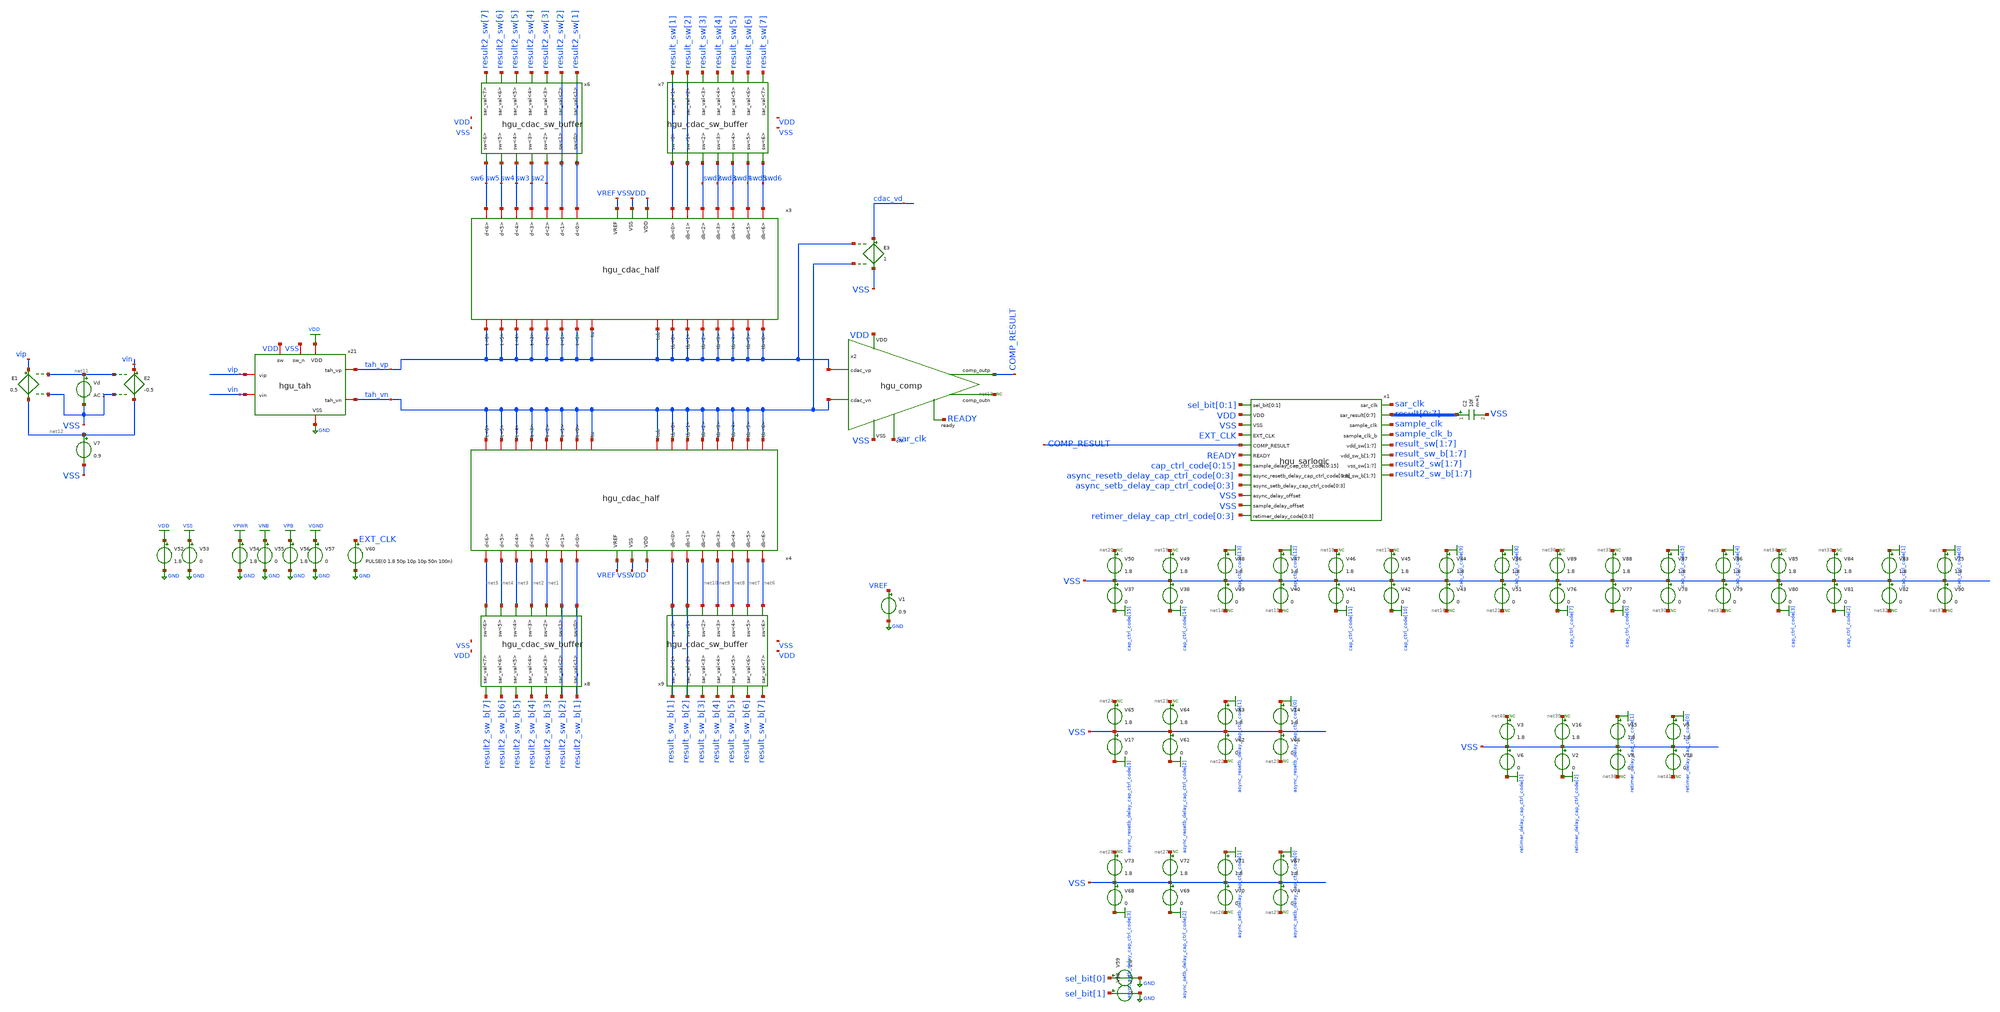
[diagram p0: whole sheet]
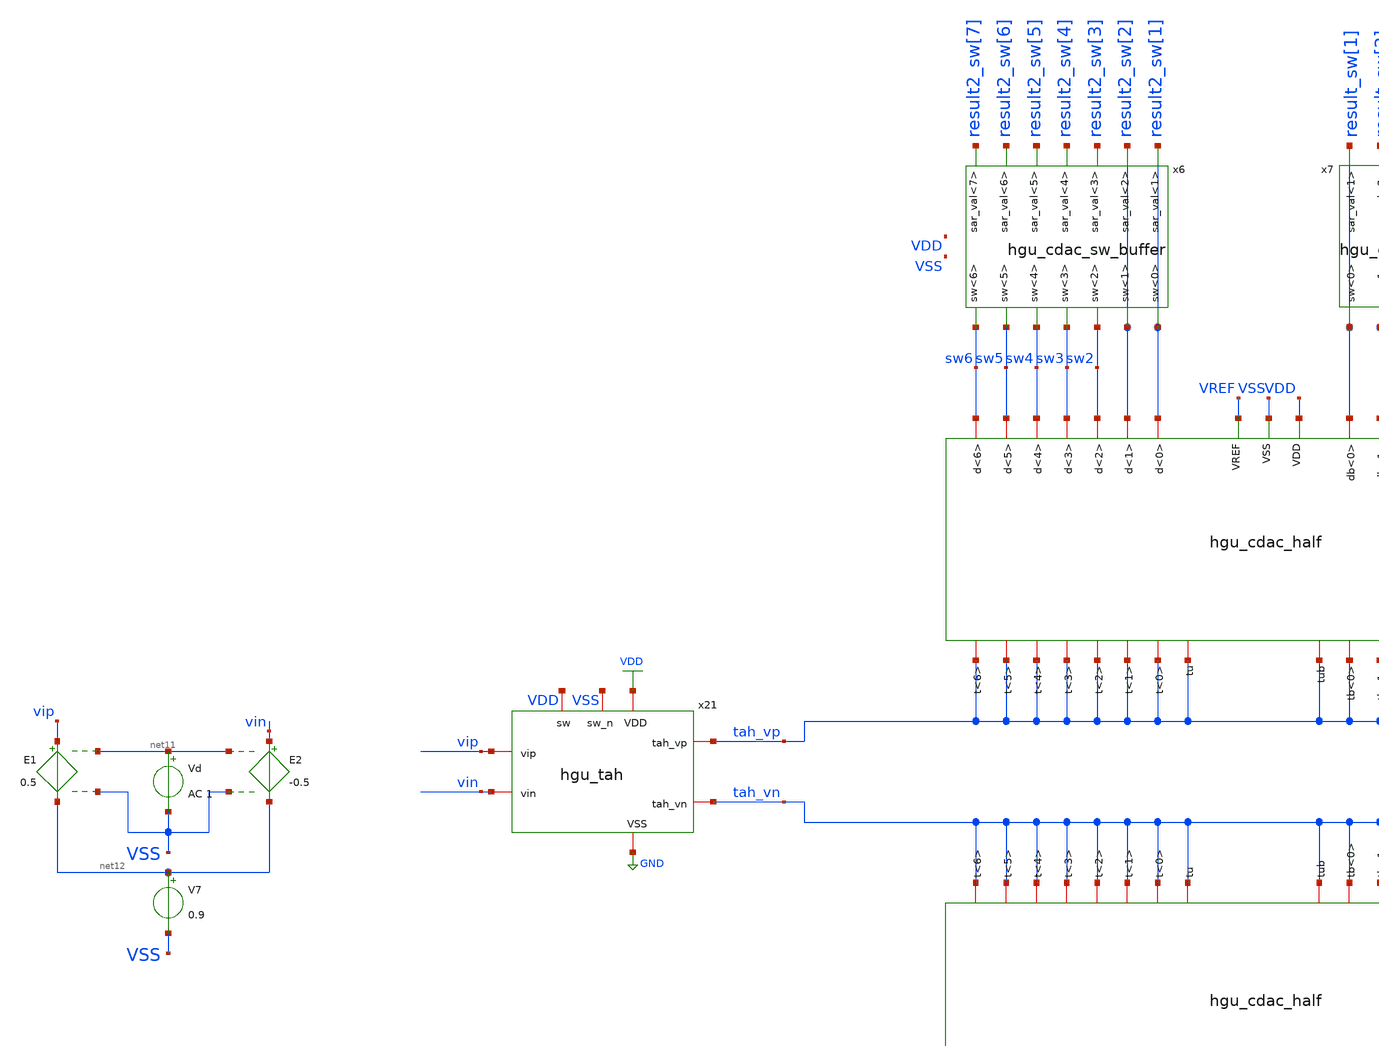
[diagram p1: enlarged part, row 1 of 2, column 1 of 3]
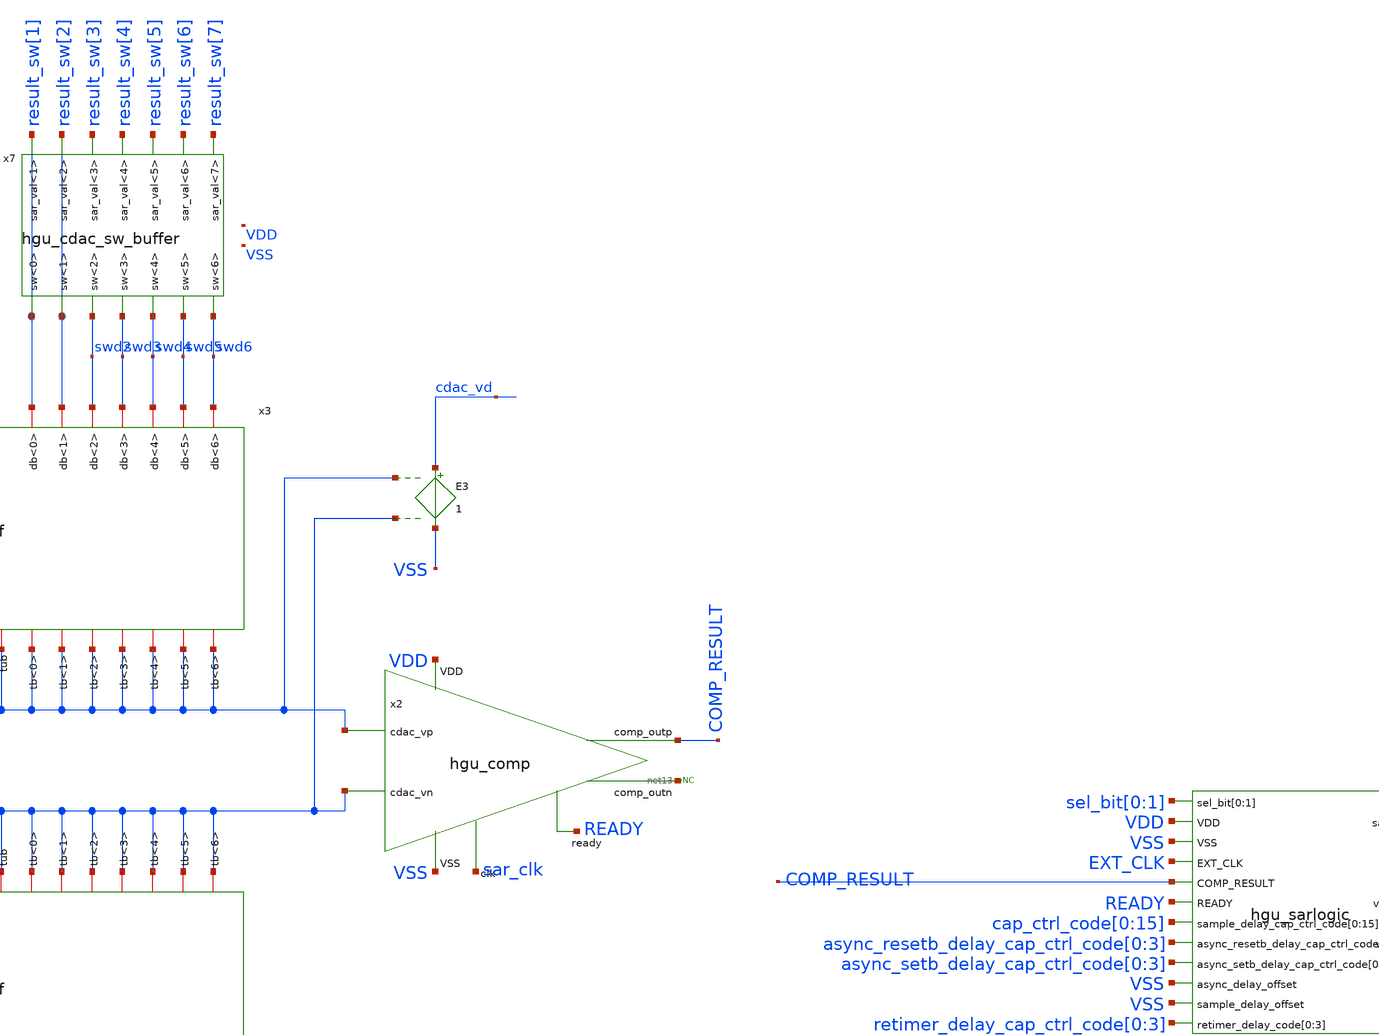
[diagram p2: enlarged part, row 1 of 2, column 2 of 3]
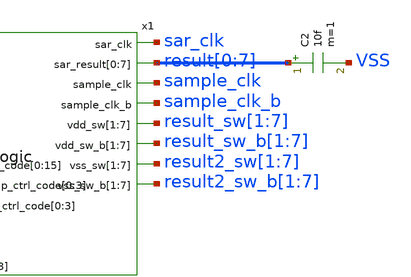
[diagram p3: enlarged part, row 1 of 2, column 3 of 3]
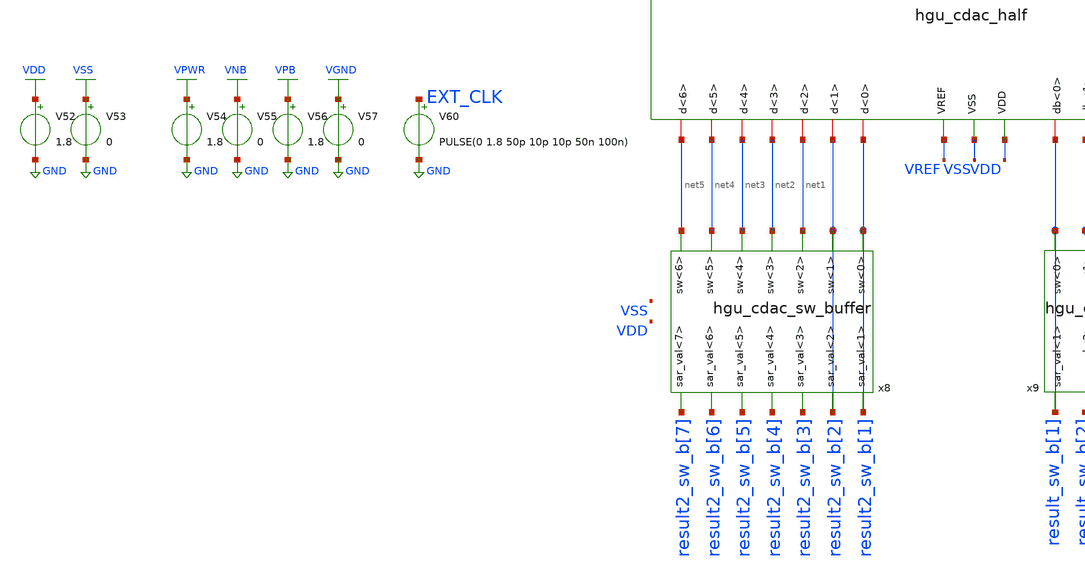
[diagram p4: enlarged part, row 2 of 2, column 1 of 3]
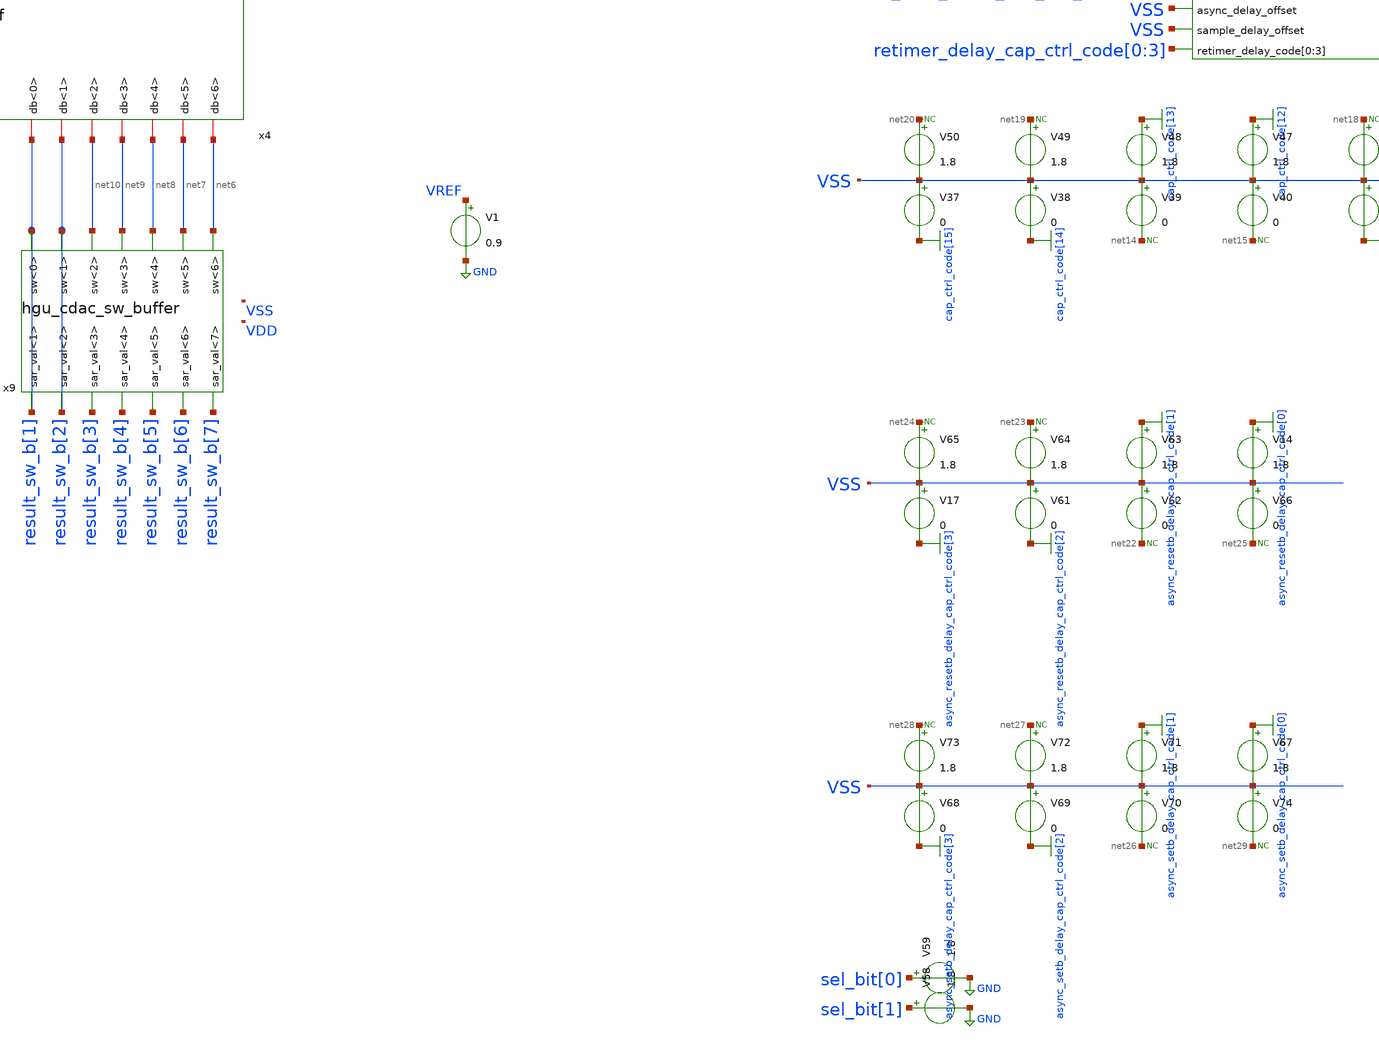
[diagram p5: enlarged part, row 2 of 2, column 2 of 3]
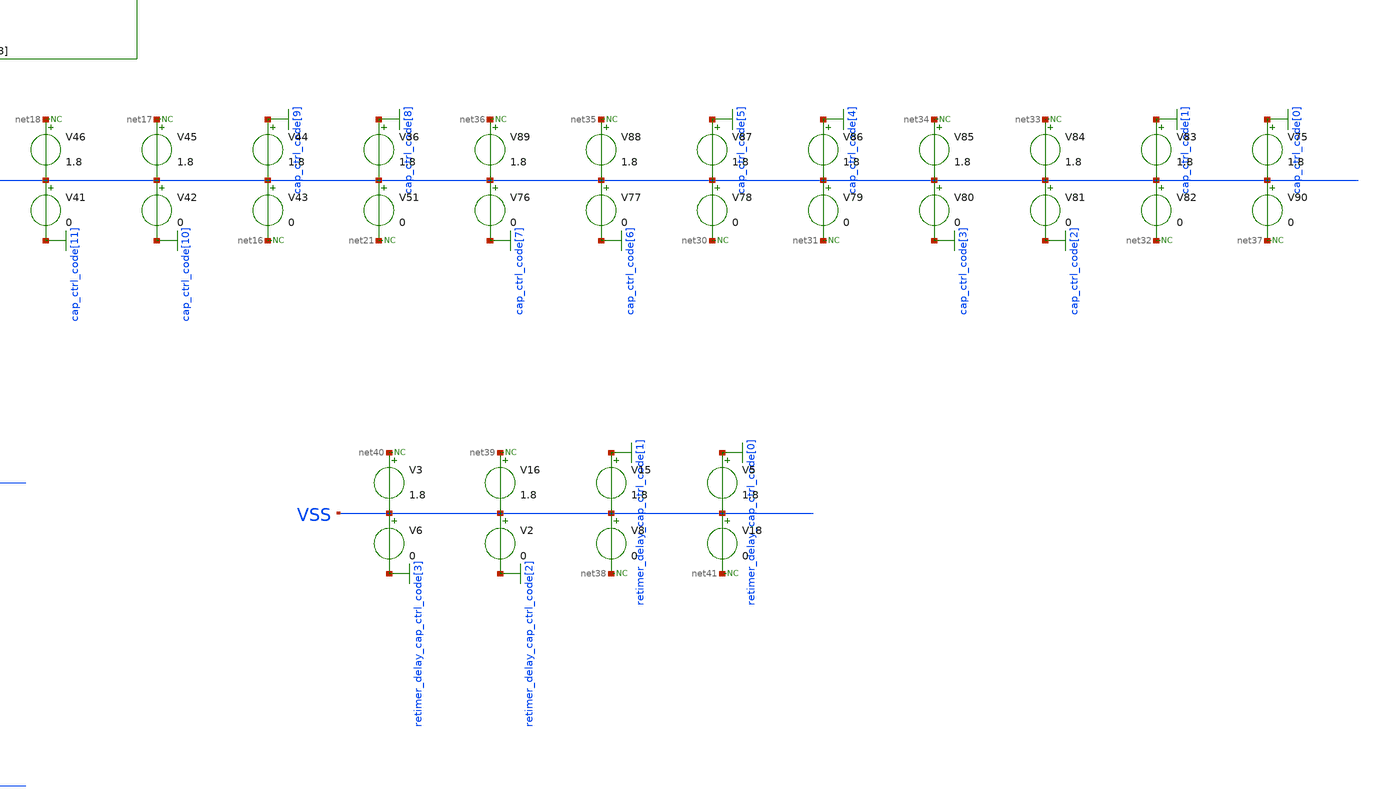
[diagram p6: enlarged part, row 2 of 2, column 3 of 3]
** sch_path: hgu/tb/tb_hgu_AC.sch
**.subckt tb_hgu_AC
x2 READY tah_vn COMP_RESULT net13 tah_vp sar_clk VDD VSS hgu_comp
x3 sw5 swd4 sw3 result_sw[2] swd2 sw2 swd6 swd5 result_sw[1] sw4 sw6 result2_sw[2] result2_sw[1]
+ swd3 VSS VREF tah_vp tah_vp tah_vp tah_vp tah_vp tah_vp tah_vp tah_vp tah_vp tah_vp tah_vp tah_vp tah_vp
+ tah_vp tah_vp tah_vp VDD hgu_cdac_half
x4 net4 net8 net2 result_sw_b[2] net10 net1 net6 net7 result_sw_b[1] net3 net5 result2_sw_b[2]
+ result2_sw_b[1] net9 VSS VREF tah_vn tah_vn tah_vn tah_vn tah_vn tah_vn tah_vn tah_vn tah_vn tah_vn tah_vn tah_vn
+ tah_vn tah_vn tah_vn tah_vn VDD hgu_cdac_half
x21 VDD VDD GND VSS tah_vp vip vin tah_vn hgu_tah
V52 VDD GND 1.8
V53 VSS GND 0
V54 VPWR GND 1.8
V55 VNB GND 0
V56 VPB GND 1.8
V57 VGND GND 0
V60 EXT_CLK GND PULSE(0 1.8 50p 10p 10p 50n 100n)
x6 result2_sw[3] result2_sw[6] result2_sw[1] result2_sw[2] result2_sw[4] result2_sw[5] result2_sw[7]
+ result2_sw[2] sw2 sw5 sw3 result2_sw[1] sw4 sw6 hgu_cdac_sw_buffer
x7 result_sw[3] result_sw[6] result_sw[1] result_sw[2] result_sw[4] result_sw[5] result_sw[7]
+ result_sw[2] swd2 swd5 swd3 result_sw[1] swd4 swd6 hgu_cdac_sw_buffer
x8 result2_sw_b[3] result2_sw_b[6] result2_sw_b[1] result2_sw_b[2] result2_sw_b[4] result2_sw_b[5]
+ result2_sw_b[7] result2_sw_b[2] net1 net4 net2 result2_sw_b[1] net3 net5 hgu_cdac_sw_buffer
x9 result_sw_b[3] result_sw_b[6] result_sw_b[1] result_sw_b[2] result_sw_b[4] result_sw_b[5]
+ result_sw_b[7] result_sw_b[2] net10 net7 net9 result_sw_b[1] net8 net6 hgu_cdac_sw_buffer
V1 VREF GND 0.9
E1 vip net12 net11 VSS 0.5
E2 vin net12 net11 VSS -0.5
Vd net11 VSS AC 1
V7 net12 VSS 0.9
E3 cdac_vd VSS tah_vp tah_vn 1
x1 sar_clk result[0] result[1] result[2] result[3] result[4] result[5] result[6] result[7]
+ sample_clk sel_bit[0] sel_bit[1] sample_clk_b VDD VSS EXT_CLK COMP_RESULT READY result_sw[1] result_sw[2]
+ result_sw[3] result_sw[4] result_sw[5] result_sw[6] result_sw[7] result_sw_b[1] result_sw_b[2] result_sw_b[3]
+ result_sw_b[4] result_sw_b[5] result_sw_b[6] result_sw_b[7] result2_sw[1] result2_sw[2] result2_sw[3]
+ result2_sw[4] result2_sw[5] result2_sw[6] result2_sw[7] result2_sw_b[1] result2_sw_b[2] result2_sw_b[3]
+ result2_sw_b[4] result2_sw_b[5] result2_sw_b[6] result2_sw_b[7] cap_ctrl_code[0] cap_ctrl_code[1] cap_ctrl_code[2]
+ cap_ctrl_code[3] cap_ctrl_code[4] cap_ctrl_code[5] cap_ctrl_code[6] cap_ctrl_code[7] cap_ctrl_code[8]
+ cap_ctrl_code[9] cap_ctrl_code[10] cap_ctrl_code[11] cap_ctrl_code[12] cap_ctrl_code[13] cap_ctrl_code[14]
+ cap_ctrl_code[15] async_resetb_delay_cap_ctrl_code[0] async_resetb_delay_cap_ctrl_code[1]
+ async_resetb_delay_cap_ctrl_code[2] async_resetb_delay_cap_ctrl_code[3] async_setb_delay_cap_ctrl_code[0]
+ async_setb_delay_cap_ctrl_code[1] async_setb_delay_cap_ctrl_code[2] async_setb_delay_cap_ctrl_code[3] VSS VSS
+ retimer_delay_cap_ctrl_code[0] retimer_delay_cap_ctrl_code[1] retimer_delay_cap_ctrl_code[2] retimer_delay_cap_ctrl_code[3]
+ hgu_sarlogic
* noconn #net13
C2 result[0] VSS 10f m=1
V36 cap_ctrl_code[8] VSS 1.8
V37 VSS cap_ctrl_code[15] 0
V38 VSS cap_ctrl_code[14] 0
V39 VSS net14 0
V40 VSS net15 0
V41 VSS cap_ctrl_code[11] 0
V42 VSS cap_ctrl_code[10] 0
V43 VSS net16 0
V44 cap_ctrl_code[9] VSS 1.8
V45 net17 VSS 1.8
V46 net18 VSS 1.8
V47 cap_ctrl_code[12] VSS 1.8
V48 cap_ctrl_code[13] VSS 1.8
V49 net19 VSS 1.8
V50 net20 VSS 1.8
V51 VSS net21 0
* noconn #net20
* noconn #net19
* noconn #net14
* noconn #net15
* noconn #net18
* noconn #net17
* noconn #net16
* noconn #net21
V58 sel_bit[1] GND 1.8
V59 sel_bit[0] GND 1.8
V14 async_resetb_delay_cap_ctrl_code[0] VSS 1.8
V17 VSS async_resetb_delay_cap_ctrl_code[3] 0
V61 VSS async_resetb_delay_cap_ctrl_code[2] 0
V62 VSS net22 0
V63 async_resetb_delay_cap_ctrl_code[1] VSS 1.8
V64 net23 VSS 1.8
V65 net24 VSS 1.8
V66 VSS net25 0
* noconn #net24
* noconn #net23
* noconn #net22
* noconn #net25
V67 async_setb_delay_cap_ctrl_code[0] VSS 1.8
V68 VSS async_setb_delay_cap_ctrl_code[3] 0
V69 VSS async_setb_delay_cap_ctrl_code[2] 0
V70 VSS net26 0
V71 async_setb_delay_cap_ctrl_code[1] VSS 1.8
V72 net27 VSS 1.8
V73 net28 VSS 1.8
V74 VSS net29 0
* noconn #net28
* noconn #net27
* noconn #net26
* noconn #net29
V75 cap_ctrl_code[0] VSS 1.8
V76 VSS cap_ctrl_code[7] 0
V77 VSS cap_ctrl_code[6] 0
V78 VSS net30 0
V79 VSS net31 0
V80 VSS cap_ctrl_code[3] 0
V81 VSS cap_ctrl_code[2] 0
V82 VSS net32 0
V83 cap_ctrl_code[1] VSS 1.8
V84 net33 VSS 1.8
V85 net34 VSS 1.8
V86 cap_ctrl_code[4] VSS 1.8
V87 cap_ctrl_code[5] VSS 1.8
V88 net35 VSS 1.8
V89 net36 VSS 1.8
V90 VSS net37 0
* noconn #net36
* noconn #net35
* noconn #net30
* noconn #net31
* noconn #net34
* noconn #net33
* noconn #net32
* noconn #net37
V5 retimer_delay_cap_ctrl_code[0] VSS 1.8
V6 VSS retimer_delay_cap_ctrl_code[3] 0
V2 VSS retimer_delay_cap_ctrl_code[2] 0
V8 VSS net38 0
V15 retimer_delay_cap_ctrl_code[1] VSS 1.8
V16 net39 VSS 1.8
V3 net40 VSS 1.8
V18 VSS net41 0
* noconn #net40
* noconn #net39
* noconn #net38
* noconn #net41
**** begin user architecture code


.lib /foss/pdks/sky130A/libs.tech/ngspice/sky130.lib.spice tt
.include /foss/pdks/sky130A/libs.ref/sky130_fd_sc_hd/spice/sky130_fd_sc_hd.spice
.include /foss/designs/hgu_goss/hgu/mag/hgu_cdac_unit.spice
.include /foss/designs/hgu_goss/hgu/spice/hgu_comp_flat_RC.spice
.include /foss/designs/hgu_goss/hgu/spice/hgu_sarlogic_8bit_logic_flat_RC.spice
.OPTIONS savecurrents
.control
  save all
  ac dec 10 1 1e9
  remzerovec
  write ac_top.raw
  plot vdb(cdac_vd)
  plot ph(cdac_vd)
.endc



**** end user architecture code
**.ends
.GLOBAL GND
.GLOBAL VDD
.GLOBAL VSS
.GLOBAL VGND
.GLOBAL VNB
.GLOBAL VPB
.GLOBAL VPWR
.GLOBAL cap_ctrl_code[15]
.GLOBAL cap_ctrl_code[14]
.GLOBAL cap_ctrl_code[13]
.GLOBAL cap_ctrl_code[12]
.GLOBAL cap_ctrl_code[11]
.GLOBAL cap_ctrl_code[10]
.GLOBAL cap_ctrl_code[9]
.GLOBAL cap_ctrl_code[8]
.GLOBAL async_resetb_delay_cap_ctrl_code[3]
.GLOBAL async_resetb_delay_cap_ctrl_code[2]
.GLOBAL async_resetb_delay_cap_ctrl_code[1]
.GLOBAL async_resetb_delay_cap_ctrl_code[0]
.GLOBAL async_setb_delay_cap_ctrl_code[3]
.GLOBAL async_setb_delay_cap_ctrl_code[2]
.GLOBAL async_setb_delay_cap_ctrl_code[1]
.GLOBAL async_setb_delay_cap_ctrl_code[0]
.GLOBAL cap_ctrl_code[7]
.GLOBAL cap_ctrl_code[6]
.GLOBAL cap_ctrl_code[5]
.GLOBAL cap_ctrl_code[4]
.GLOBAL cap_ctrl_code[3]
.GLOBAL cap_ctrl_code[2]
.GLOBAL cap_ctrl_code[1]
.GLOBAL cap_ctrl_code[0]
.GLOBAL retimer_delay_cap_ctrl_code[3]
.GLOBAL retimer_delay_cap_ctrl_code[2]
.GLOBAL retimer_delay_cap_ctrl_code[1]
.GLOBAL retimer_delay_cap_ctrl_code[0]
.end
